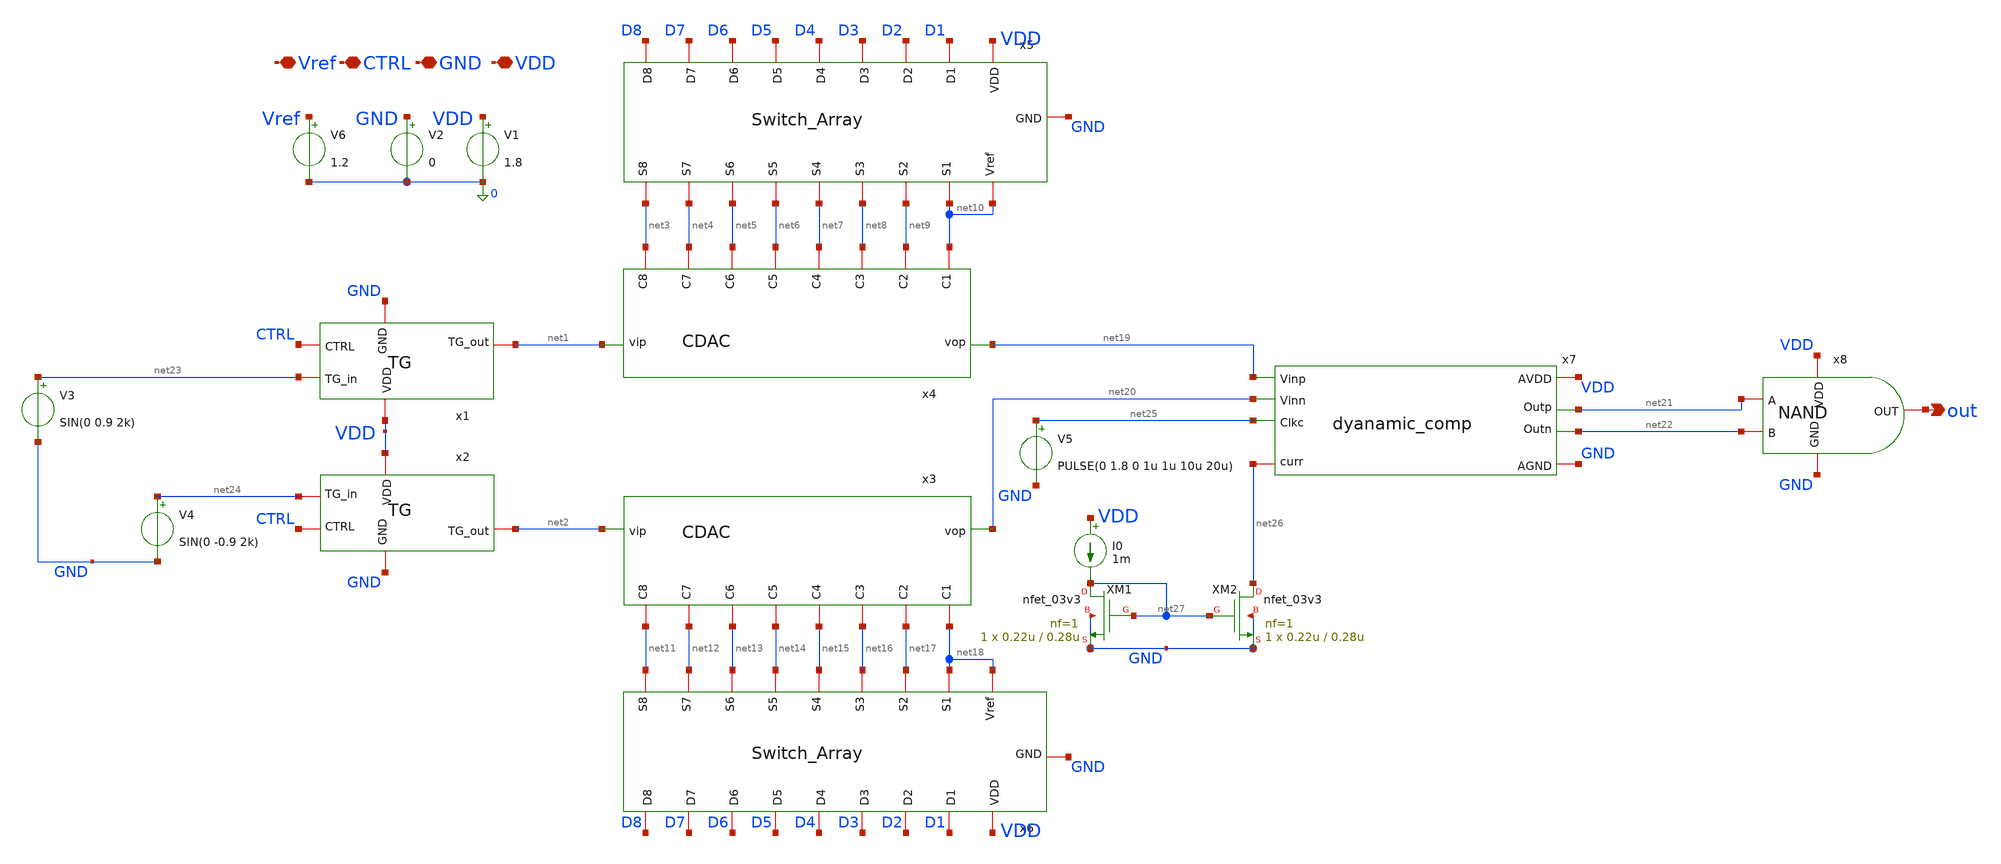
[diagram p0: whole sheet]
** sch_path: xschem/SAR-ADC.sch
**.subckt SAR-ADC VDD GND CTRL out Vref
*.iopin VDD
*.iopin GND
*.iopin CTRL
*.opin out
*.iopin Vref
x1 VDD GND net23 net1 CTRL TG
x2 VDD GND net24 net2 CTRL TG
x3 net2 net20 net13 net15 net16 net17 net18 net14 net12 net11 CDAC
x4 net1 net19 net5 net7 net8 net9 net10 net6 net4 net3 CDAC
x5 GND VDD net10 net9 net10 net8 D2 D3 D1 net5 net6 net7 D6 D5 D4 net3 net4 D8 D7 Switch_Array
x6 GND VDD net18 net17 net18 net16 D2 D3 D1 net13 net14 net15 D6 D5 D4 net11 net12 D8 D7
+ Switch_Array
x7 VDD net26 net20 net19 net22 net21 net25 GND dyanamic_comp
V1 VDD 0 1.8
V2 GND 0 0
x8 VDD net21 out net22 GND NAND
V3 net23 GND SIN(0 0.9 2k)
V4 net24 GND SIN(0 -0.9 2k)
V5 net25 GND PULSE(0 1.8 0 1u 1u 10u 20u)
XM1 net27 net27 GND GND nfet_03v3 L=0.28u W=0.22u nf=1 ad='int((nf+1)/2) * W/nf * 0.18u' as='int((nf+2)/2) * W/nf * 0.18u'
+ pd='2*int((nf+1)/2) * (W/nf + 0.18u)' ps='2*int((nf+2)/2) * (W/nf + 0.18u)' nrd='0.18u / W' nrs='0.18u / W'
+ sa=0 sb=0 sd=0 m=1
XM2 net26 net27 GND GND nfet_03v3 L=0.28u W=0.22u nf=1 ad='int((nf+1)/2) * W/nf * 0.18u' as='int((nf+2)/2) * W/nf * 0.18u'
+ pd='2*int((nf+1)/2) * (W/nf + 0.18u)' ps='2*int((nf+2)/2) * (W/nf + 0.18u)' nrd='0.18u / W' nrs='0.18u / W'
+ sa=0 sb=0 sd=0 m=1
I0 VDD net27 1m
V6 Vref 0 1.2
**.ends

* expanding   symbol:  TG.sym # of pins=5
** sym_path: xschem/TG.sym
** sch_path: xschem/TG.sch
.subckt TG VDD GND TG_in TG_out CTRL
*.iopin TG_in
*.iopin TG_out
*.iopin VDD
*.iopin GND
*.iopin CTRL
XM1 TG_out net1 TG_in VDD pfet_03v3 L=0.28u W=0.55u nf=1 ad='int((nf+1)/2) * W/nf * 0.18u' as='int((nf+2)/2) * W/nf * 0.18u'
+ pd='2*int((nf+1)/2) * (W/nf + 0.18u)' ps='2*int((nf+2)/2) * (W/nf + 0.18u)' nrd='0.18u / W' nrs='0.18u / W'
+ sa=0 sb=0 sd=0 m=1
XM2 TG_out CTRL TG_in GND nfet_03v3 L=0.28u W=0.22u nf=1 ad='int((nf+1)/2) * W/nf * 0.18u' as='int((nf+2)/2) * W/nf * 0.18u'
+ pd='2*int((nf+1)/2) * (W/nf + 0.18u)' ps='2*int((nf+2)/2) * (W/nf + 0.18u)' nrd='0.18u / W' nrs='0.18u / W'
+ sa=0 sb=0 sd=0 m=1
x1 VDD CTRL net1 GND inv
.ends


* expanding   symbol:  CDAC.sym # of pins=10
** sym_path: xschem/CDAC.sym
** sch_path: xschem/CDAC.sch
.subckt CDAC vip vop C6 C4 C3 C2 C1 C5 C7 C8
*.iopin C8
*.iopin C7
*.iopin C6
*.iopin C5
*.iopin C4
*.iopin C3
*.iopin C2
*.iopin C1
*.opin vop
*.ipin vip
XC1 vop C8 cap_mim_2f0fF c_width=1e-6 c_length=1e-6 m=64
XC2 vop C8 cap_mim_2f0fF c_width=1e-6 c_length=1e-6 m=64
XC3 vop C7 cap_mim_2f0fF c_width=1e-6 c_length=1e-6 m=32
XC4 vop C7 cap_mim_2f0fF c_width=1e-6 c_length=1e-6 m=32
XC5 vop C6 cap_mim_2f0fF c_width=1e-6 c_length=1e-6 m=16
XC6 vop C6 cap_mim_2f0fF c_width=1e-6 c_length=1e-6 m=16
R1 vip vop 1k m=1
XC7 vop C5 cap_mim_2f0fF c_width=1e-6 c_length=1e-6 m=8
XC8 vop C5 cap_mim_2f0fF c_width=1e-6 c_length=1e-6 m=8
XC9 vop C4 cap_mim_2f0fF c_width=1e-6 c_length=1e-6 m=4
XC10 vop C4 cap_mim_2f0fF c_width=1e-6 c_length=1e-6 m=4
XC11 vop C3 cap_mim_2f0fF c_width=1e-6 c_length=1e-6 m=2
XC12 vop C3 cap_mim_2f0fF c_width=1e-6 c_length=1e-6 m=2
XC13 vop C2 cap_mim_2f0fF c_width=1e-6 c_length=1e-6 m=1
XC14 vop C2 cap_mim_2f0fF c_width=1e-6 c_length=1e-6 m=1
XC15 vop C1 cap_mim_2f0fF c_width=1e-6 c_length=1e-6 m=1
XC16 vop C1 cap_mim_2f0fF c_width=1e-6 c_length=1e-6 m=1
.ends


* expanding   symbol:  Switch_Array.sym # of pins=19
** sym_path: xschem/Switch_Array.sym
** sch_path: xschem/Switch_Array.sch
.subckt Switch_Array GND VDD Vref S2 S1 S3 D2 D3 D1 S6 S5 S4 D6 D5 D4 S8 S7 D8 D7
*.iopin VDD
*.iopin GND
*.iopin Vref
*.iopin S1
*.iopin D1
*.iopin S2
*.iopin D2
*.iopin S3
*.iopin D3
*.iopin S4
*.iopin D4
*.iopin S5
*.iopin D5
*.iopin S6
*.iopin D6
*.iopin S7
*.iopin D7
*.iopin S8
*.iopin D8
XM3 S1 net9 GND GND nfet_03v3 L=0.28u W=0.22u nf=1 ad='int((nf+1)/2) * W/nf * 0.18u' as='int((nf+2)/2) * W/nf * 0.18u'
+ pd='2*int((nf+1)/2) * (W/nf + 0.18u)' ps='2*int((nf+2)/2) * (W/nf + 0.18u)' nrd='0.18u / W' nrs='0.18u / W'
+ sa=0 sb=0 sd=0 m=1
x2 VDD D1 net9 GND inv
XM1 S1 net1 Vref VDD pfet_03v3 L=0.28u W=0.55u nf=1 ad='int((nf+1)/2) * W/nf * 0.18u' as='int((nf+2)/2) * W/nf * 0.18u'
+ pd='2*int((nf+1)/2) * (W/nf + 0.18u)' ps='2*int((nf+2)/2) * (W/nf + 0.18u)' nrd='0.18u / W' nrs='0.18u / W'
+ sa=0 sb=0 sd=0 m=1
XM4 S1 D1 Vref GND nfet_03v3 L=0.28u W=0.22u nf=1 ad='int((nf+1)/2) * W/nf * 0.18u' as='int((nf+2)/2) * W/nf * 0.18u'
+ pd='2*int((nf+1)/2) * (W/nf + 0.18u)' ps='2*int((nf+2)/2) * (W/nf + 0.18u)' nrd='0.18u / W' nrs='0.18u / W'
+ sa=0 sb=0 sd=0 m=1
x1 VDD D1 net1 GND inv
x3 VDD D2 net10 GND inv
XM7 S2 net2 Vref VDD pfet_03v3 L=0.28u W=0.55u nf=1 ad='int((nf+1)/2) * W/nf * 0.18u' as='int((nf+2)/2) * W/nf * 0.18u'
+ pd='2*int((nf+1)/2) * (W/nf + 0.18u)' ps='2*int((nf+2)/2) * (W/nf + 0.18u)' nrd='0.18u / W' nrs='0.18u / W'
+ sa=0 sb=0 sd=0 m=1
XM8 S2 D2 Vref GND nfet_03v3 L=0.28u W=0.22u nf=1 ad='int((nf+1)/2) * W/nf * 0.18u' as='int((nf+2)/2) * W/nf * 0.18u'
+ pd='2*int((nf+1)/2) * (W/nf + 0.18u)' ps='2*int((nf+2)/2) * (W/nf + 0.18u)' nrd='0.18u / W' nrs='0.18u / W'
+ sa=0 sb=0 sd=0 m=1
x4 VDD D2 net2 GND inv
XM11 S3 net3 Vref VDD pfet_03v3 L=0.28u W=0.55u nf=1 ad='int((nf+1)/2) * W/nf * 0.18u' as='int((nf+2)/2) * W/nf * 0.18u'
+ pd='2*int((nf+1)/2) * (W/nf + 0.18u)' ps='2*int((nf+2)/2) * (W/nf + 0.18u)' nrd='0.18u / W' nrs='0.18u / W'
+ sa=0 sb=0 sd=0 m=1
XM12 S3 D3 Vref GND nfet_03v3 L=0.28u W=0.22u nf=1 ad='int((nf+1)/2) * W/nf * 0.18u' as='int((nf+2)/2) * W/nf * 0.18u'
+ pd='2*int((nf+1)/2) * (W/nf + 0.18u)' ps='2*int((nf+2)/2) * (W/nf + 0.18u)' nrd='0.18u / W' nrs='0.18u / W'
+ sa=0 sb=0 sd=0 m=1
x6 VDD D3 net3 GND inv
XM15 S4 net4 Vref VDD pfet_03v3 L=0.28u W=0.55u nf=1 ad='int((nf+1)/2) * W/nf * 0.18u' as='int((nf+2)/2) * W/nf * 0.18u'
+ pd='2*int((nf+1)/2) * (W/nf + 0.18u)' ps='2*int((nf+2)/2) * (W/nf + 0.18u)' nrd='0.18u / W' nrs='0.18u / W'
+ sa=0 sb=0 sd=0 m=1
XM16 S4 D4 Vref GND nfet_03v3 L=0.28u W=0.22u nf=1 ad='int((nf+1)/2) * W/nf * 0.18u' as='int((nf+2)/2) * W/nf * 0.18u'
+ pd='2*int((nf+1)/2) * (W/nf + 0.18u)' ps='2*int((nf+2)/2) * (W/nf + 0.18u)' nrd='0.18u / W' nrs='0.18u / W'
+ sa=0 sb=0 sd=0 m=1
x8 VDD D4 net4 GND inv
XM19 S5 net5 Vref VDD pfet_03v3 L=0.28u W=0.55u nf=1 ad='int((nf+1)/2) * W/nf * 0.18u' as='int((nf+2)/2) * W/nf * 0.18u'
+ pd='2*int((nf+1)/2) * (W/nf + 0.18u)' ps='2*int((nf+2)/2) * (W/nf + 0.18u)' nrd='0.18u / W' nrs='0.18u / W'
+ sa=0 sb=0 sd=0 m=1
XM20 S5 D5 Vref GND nfet_03v3 L=0.28u W=0.22u nf=1 ad='int((nf+1)/2) * W/nf * 0.18u' as='int((nf+2)/2) * W/nf * 0.18u'
+ pd='2*int((nf+1)/2) * (W/nf + 0.18u)' ps='2*int((nf+2)/2) * (W/nf + 0.18u)' nrd='0.18u / W' nrs='0.18u / W'
+ sa=0 sb=0 sd=0 m=1
x10 VDD D5 net5 GND inv
XM23 S6 net6 Vref VDD pfet_03v3 L=0.28u W=0.55u nf=1 ad='int((nf+1)/2) * W/nf * 0.18u' as='int((nf+2)/2) * W/nf * 0.18u'
+ pd='2*int((nf+1)/2) * (W/nf + 0.18u)' ps='2*int((nf+2)/2) * (W/nf + 0.18u)' nrd='0.18u / W' nrs='0.18u / W'
+ sa=0 sb=0 sd=0 m=1
XM24 S6 D6 Vref GND nfet_03v3 L=0.28u W=0.22u nf=1 ad='int((nf+1)/2) * W/nf * 0.18u' as='int((nf+2)/2) * W/nf * 0.18u'
+ pd='2*int((nf+1)/2) * (W/nf + 0.18u)' ps='2*int((nf+2)/2) * (W/nf + 0.18u)' nrd='0.18u / W' nrs='0.18u / W'
+ sa=0 sb=0 sd=0 m=1
x12 VDD D6 net6 GND inv
XM27 S7 net7 Vref VDD pfet_03v3 L=0.28u W=0.55u nf=1 ad='int((nf+1)/2) * W/nf * 0.18u' as='int((nf+2)/2) * W/nf * 0.18u'
+ pd='2*int((nf+1)/2) * (W/nf + 0.18u)' ps='2*int((nf+2)/2) * (W/nf + 0.18u)' nrd='0.18u / W' nrs='0.18u / W'
+ sa=0 sb=0 sd=0 m=1
XM28 S7 D7 Vref GND nfet_03v3 L=0.28u W=0.22u nf=1 ad='int((nf+1)/2) * W/nf * 0.18u' as='int((nf+2)/2) * W/nf * 0.18u'
+ pd='2*int((nf+1)/2) * (W/nf + 0.18u)' ps='2*int((nf+2)/2) * (W/nf + 0.18u)' nrd='0.18u / W' nrs='0.18u / W'
+ sa=0 sb=0 sd=0 m=1
x14 VDD D7 net7 GND inv
XM31 S8 net8 Vref VDD pfet_03v3 L=0.28u W=0.55u nf=1 ad='int((nf+1)/2) * W/nf * 0.18u' as='int((nf+2)/2) * W/nf * 0.18u'
+ pd='2*int((nf+1)/2) * (W/nf + 0.18u)' ps='2*int((nf+2)/2) * (W/nf + 0.18u)' nrd='0.18u / W' nrs='0.18u / W'
+ sa=0 sb=0 sd=0 m=1
XM32 S8 D8 Vref GND nfet_03v3 L=0.28u W=0.22u nf=1 ad='int((nf+1)/2) * W/nf * 0.18u' as='int((nf+2)/2) * W/nf * 0.18u'
+ pd='2*int((nf+1)/2) * (W/nf + 0.18u)' ps='2*int((nf+2)/2) * (W/nf + 0.18u)' nrd='0.18u / W' nrs='0.18u / W'
+ sa=0 sb=0 sd=0 m=1
x16 VDD D8 net8 GND inv
XM2 S2 net10 GND GND nfet_03v3 L=0.28u W=0.22u nf=1 ad='int((nf+1)/2) * W/nf * 0.18u' as='int((nf+2)/2) * W/nf * 0.18u'
+ pd='2*int((nf+1)/2) * (W/nf + 0.18u)' ps='2*int((nf+2)/2) * (W/nf + 0.18u)' nrd='0.18u / W' nrs='0.18u / W'
+ sa=0 sb=0 sd=0 m=1
x5 VDD D3 net11 GND inv
XM5 S3 net11 GND GND nfet_03v3 L=0.28u W=0.22u nf=1 ad='int((nf+1)/2) * W/nf * 0.18u' as='int((nf+2)/2) * W/nf * 0.18u'
+ pd='2*int((nf+1)/2) * (W/nf + 0.18u)' ps='2*int((nf+2)/2) * (W/nf + 0.18u)' nrd='0.18u / W' nrs='0.18u / W'
+ sa=0 sb=0 sd=0 m=1
XM6 S4 net12 GND GND nfet_03v3 L=0.28u W=0.22u nf=1 ad='int((nf+1)/2) * W/nf * 0.18u' as='int((nf+2)/2) * W/nf * 0.18u'
+ pd='2*int((nf+1)/2) * (W/nf + 0.18u)' ps='2*int((nf+2)/2) * (W/nf + 0.18u)' nrd='0.18u / W' nrs='0.18u / W'
+ sa=0 sb=0 sd=0 m=1
x7 VDD D4 net12 GND inv
XM9 S5 net13 GND GND nfet_03v3 L=0.28u W=0.22u nf=1 ad='int((nf+1)/2) * W/nf * 0.18u' as='int((nf+2)/2) * W/nf * 0.18u'
+ pd='2*int((nf+1)/2) * (W/nf + 0.18u)' ps='2*int((nf+2)/2) * (W/nf + 0.18u)' nrd='0.18u / W' nrs='0.18u / W'
+ sa=0 sb=0 sd=0 m=1
x9 VDD D5 net13 GND inv
XM10 S6 net14 GND GND nfet_03v3 L=0.28u W=0.22u nf=1 ad='int((nf+1)/2) * W/nf * 0.18u' as='int((nf+2)/2) * W/nf * 0.18u'
+ pd='2*int((nf+1)/2) * (W/nf + 0.18u)' ps='2*int((nf+2)/2) * (W/nf + 0.18u)' nrd='0.18u / W' nrs='0.18u / W'
+ sa=0 sb=0 sd=0 m=1
x11 VDD D6 net14 GND inv
XM13 S7 net15 GND GND nfet_03v3 L=0.28u W=0.22u nf=1 ad='int((nf+1)/2) * W/nf * 0.18u' as='int((nf+2)/2) * W/nf * 0.18u'
+ pd='2*int((nf+1)/2) * (W/nf + 0.18u)' ps='2*int((nf+2)/2) * (W/nf + 0.18u)' nrd='0.18u / W' nrs='0.18u / W'
+ sa=0 sb=0 sd=0 m=1
x13 VDD D7 net15 GND inv
XM14 S8 net16 GND GND nfet_03v3 L=0.28u W=0.22u nf=1 ad='int((nf+1)/2) * W/nf * 0.18u' as='int((nf+2)/2) * W/nf * 0.18u'
+ pd='2*int((nf+1)/2) * (W/nf + 0.18u)' ps='2*int((nf+2)/2) * (W/nf + 0.18u)' nrd='0.18u / W' nrs='0.18u / W'
+ sa=0 sb=0 sd=0 m=1
x15 VDD D8 net16 GND inv
.ends


* expanding   symbol:  dyanamic_comp.sym # of pins=8
** sym_path: xschem/dyanamic_comp.sym
** sch_path: xschem/dyanamic_comp.sch
.subckt dyanamic_comp AVDD curr Vinn Vinp Outn Outp Clkc AGND
*.iopin AVDD
*.iopin curr
*.opin Outp
*.ipin Clkc
*.iopin AGND
*.opin Outn
*.ipin Vinp
*.ipin Vinn
XMP1 net3 Vinp net2 AVDD pfet_03v3 L=2u W=2u nf=1 ad='int((nf+1)/2) * W/nf * 0.18u' as='int((nf+2)/2) * W/nf * 0.18u'
+ pd='2*int((nf+1)/2) * (W/nf + 0.18u)' ps='2*int((nf+2)/2) * (W/nf + 0.18u)' nrd='0.18u / W' nrs='0.18u / W'
+ sa=0 sb=0 sd=0 m=9
XMP2 net4 Vinn net2 AVDD pfet_03v3 L=2u W=2u nf=1 ad='int((nf+1)/2) * W/nf * 0.18u' as='int((nf+2)/2) * W/nf * 0.18u'
+ pd='2*int((nf+1)/2) * (W/nf + 0.18u)' ps='2*int((nf+2)/2) * (W/nf + 0.18u)' nrd='0.18u / W' nrs='0.18u / W'
+ sa=0 sb=0 sd=0 m=9
XMN4 net4 net3 AGND AGND nfet_03v3 L=2u W=0.6u nf=1 ad='int((nf+1)/2) * W/nf * 0.18u' as='int((nf+2)/2) * W/nf * 0.18u'
+ pd='2*int((nf+1)/2) * (W/nf + 0.18u)' ps='2*int((nf+2)/2) * (W/nf + 0.18u)' nrd='0.18u / W' nrs='0.18u / W'
+ sa=0 sb=0 sd=0 m=1
XMN5 net3 Clkc AGND AGND nfet_03v3 L=2u W=0.6u nf=1 ad='int((nf+1)/2) * W/nf * 0.18u' as='int((nf+2)/2) * W/nf * 0.18u'
+ pd='2*int((nf+1)/2) * (W/nf + 0.18u)' ps='2*int((nf+2)/2) * (W/nf + 0.18u)' nrd='0.18u / W' nrs='0.18u / W'
+ sa=0 sb=0 sd=0 m=1
XMN6 net4 Clkc AGND AGND nfet_03v3 L=2u W=0.6u nf=1 ad='int((nf+1)/2) * W/nf * 0.18u' as='int((nf+2)/2) * W/nf * 0.18u'
+ pd='2*int((nf+1)/2) * (W/nf + 0.18u)' ps='2*int((nf+2)/2) * (W/nf + 0.18u)' nrd='0.18u / W' nrs='0.18u / W'
+ sa=0 sb=0 sd=0 m=1
XMN3 net3 net4 AGND AGND nfet_03v3 L=2u W=0.6u nf=1 ad='int((nf+1)/2) * W/nf * 0.18u' as='int((nf+2)/2) * W/nf * 0.18u'
+ pd='2*int((nf+1)/2) * (W/nf + 0.18u)' ps='2*int((nf+2)/2) * (W/nf + 0.18u)' nrd='0.18u / W' nrs='0.18u / W'
+ sa=0 sb=0 sd=0 m=1
XMP7 net2 Clkc net1 AVDD pfet_03v3 L=2u W=1.12u nf=1 ad='int((nf+1)/2) * W/nf * 0.18u' as='int((nf+2)/2) * W/nf * 0.18u'
+ pd='2*int((nf+1)/2) * (W/nf + 0.18u)' ps='2*int((nf+2)/2) * (W/nf + 0.18u)' nrd='0.18u / W' nrs='0.18u / W'
+ sa=0 sb=0 sd=0 m=1
XMPB net1 curr AVDD AVDD pfet_03v3 L=2u W=1.12u nf=1 ad='int((nf+1)/2) * W/nf * 0.18u' as='int((nf+2)/2) * W/nf * 0.18u'
+ pd='2*int((nf+1)/2) * (W/nf + 0.18u)' ps='2*int((nf+2)/2) * (W/nf + 0.18u)' nrd='0.18u / W' nrs='0.18u / W'
+ sa=0 sb=0 sd=0 m=1
XMP12 curr curr AVDD AVDD pfet_03v3 L=2u W=1.12u nf=1 ad='int((nf+1)/2) * W/nf * 0.18u' as='int((nf+2)/2) * W/nf * 0.18u'
+ pd='2*int((nf+1)/2) * (W/nf + 0.18u)' ps='2*int((nf+2)/2) * (W/nf + 0.18u)' nrd='0.18u / W' nrs='0.18u / W'
+ sa=0 sb=0 sd=0 m=1
XMP10 Outn net5 AVDD AVDD pfet_03v3 L=2u W=1.12u nf=1 ad='int((nf+1)/2) * W/nf * 0.18u' as='int((nf+2)/2) * W/nf * 0.18u'
+ pd='2*int((nf+1)/2) * (W/nf + 0.18u)' ps='2*int((nf+2)/2) * (W/nf + 0.18u)' nrd='0.18u / W' nrs='0.18u / W'
+ sa=0 sb=0 sd=0 m=1
XMN11 Outn net5 AGND AGND nfet_03v3 L=2u W=0.6u nf=1 ad='int((nf+1)/2) * W/nf * 0.18u' as='int((nf+2)/2) * W/nf * 0.18u'
+ pd='2*int((nf+1)/2) * (W/nf + 0.18u)' ps='2*int((nf+2)/2) * (W/nf + 0.18u)' nrd='0.18u / W' nrs='0.18u / W'
+ sa=0 sb=0 sd=0 m=1
XMP8 Outp net3 AVDD AVDD pfet_03v3 L=2u W=1.12u nf=1 ad='int((nf+1)/2) * W/nf * 0.18u' as='int((nf+2)/2) * W/nf * 0.18u'
+ pd='2*int((nf+1)/2) * (W/nf + 0.18u)' ps='2*int((nf+2)/2) * (W/nf + 0.18u)' nrd='0.18u / W' nrs='0.18u / W'
+ sa=0 sb=0 sd=0 m=1
XMN9 Outp net3 AGND AGND nfet_03v3 L=2u W=0.6u nf=1 ad='int((nf+1)/2) * W/nf * 0.18u' as='int((nf+2)/2) * W/nf * 0.18u'
+ pd='2*int((nf+1)/2) * (W/nf + 0.18u)' ps='2*int((nf+2)/2) * (W/nf + 0.18u)' nrd='0.18u / W' nrs='0.18u / W'
+ sa=0 sb=0 sd=0 m=1
V1 net4 net5 0
.ends


* expanding   symbol:  NAND.sym # of pins=5
** sym_path: xschem/NAND.sym
** sch_path: xschem/NAND.sch
.subckt NAND VDD A OUT B GND
*.iopin OUT
*.iopin GND
*.iopin VDD
*.iopin A
*.iopin B
XM1 OUT A VDD VDD pfet_03v3 L=0.28u W=0.22u nf=1 ad='int((nf+1)/2) * W/nf * 0.18u' as='int((nf+2)/2) * W/nf * 0.18u'
+ pd='2*int((nf+1)/2) * (W/nf + 0.18u)' ps='2*int((nf+2)/2) * (W/nf + 0.18u)' nrd='0.18u / W' nrs='0.18u / W'
+ sa=0 sb=0 sd=0 m=1
XM2 OUT B VDD VDD pfet_03v3 L=0.28u W=0.22u nf=1 ad='int((nf+1)/2) * W/nf * 0.18u' as='int((nf+2)/2) * W/nf * 0.18u'
+ pd='2*int((nf+1)/2) * (W/nf + 0.18u)' ps='2*int((nf+2)/2) * (W/nf + 0.18u)' nrd='0.18u / W' nrs='0.18u / W'
+ sa=0 sb=0 sd=0 m=1
XM3 OUT A net1 GND nfet_03v3 L=0.28u W=0.22u nf=1 ad='int((nf+1)/2) * W/nf * 0.18u' as='int((nf+2)/2) * W/nf * 0.18u'
+ pd='2*int((nf+1)/2) * (W/nf + 0.18u)' ps='2*int((nf+2)/2) * (W/nf + 0.18u)' nrd='0.18u / W' nrs='0.18u / W'
+ sa=0 sb=0 sd=0 m=1
XM4 net1 B GND GND nfet_03v3 L=0.28u W=0.22u nf=1 ad='int((nf+1)/2) * W/nf * 0.18u' as='int((nf+2)/2) * W/nf * 0.18u'
+ pd='2*int((nf+1)/2) * (W/nf + 0.18u)' ps='2*int((nf+2)/2) * (W/nf + 0.18u)' nrd='0.18u / W' nrs='0.18u / W'
+ sa=0 sb=0 sd=0 m=1
.ends


* expanding   symbol:  inv.sym # of pins=4
** sym_path: xschem/inv.sym
** sch_path: xschem/inv.sch
.subckt inv VDD In Out GND
*.iopin VDD
*.iopin GND
*.ipin In
*.opin Out
XM3 Out In GND GND nfet_03v3 L=0.28u W=0.22u nf=1 ad='int((nf+1)/2) * W/nf * 0.18u' as='int((nf+2)/2) * W/nf * 0.18u'
+ pd='2*int((nf+1)/2) * (W/nf + 0.18u)' ps='2*int((nf+2)/2) * (W/nf + 0.18u)' nrd='0.18u / W' nrs='0.18u / W'
+ sa=0 sb=0 sd=0 m=1
XM2 Out In VDD VDD pfet_03v3 L=0.28u W=0.55u nf=1 ad='int((nf+1)/2) * W/nf * 0.18u' as='int((nf+2)/2) * W/nf * 0.18u'
+ pd='2*int((nf+1)/2) * (W/nf + 0.18u)' ps='2*int((nf+2)/2) * (W/nf + 0.18u)' nrd='0.18u / W' nrs='0.18u / W'
+ sa=0 sb=0 sd=0 m=1
.ends

.end
